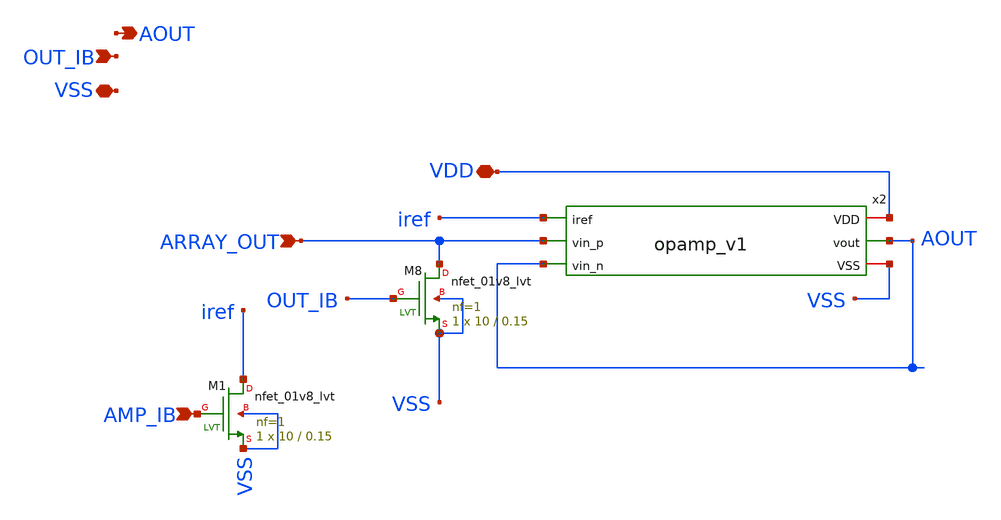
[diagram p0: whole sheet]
** sch_path: xschem/opamp_diego/opamp_wrapper.sch
**.subckt opamp_wrapper ARRAY_OUT AMP_IB VDD AOUT OUT_IB VSS
*.ipin ARRAY_OUT
*.ipin AMP_IB
*.iopin VDD
*.opin AOUT
*.ipin OUT_IB
*.iopin VSS
XM8 ARRAY_OUT OUT_IB VSS VSS sky130_fd_pr__nfet_01v8_lvt L=0.15 W=10 nf=1 ad='int((nf+1)/2) * W/nf * 0.29'
+ as='int((nf+2)/2) * W/nf * 0.29' pd='2*int((nf+1)/2) * (W/nf + 0.29)' ps='2*int((nf+2)/2) * (W/nf + 0.29)'
+ nrd='0.29 / W' nrs='0.29 / W' sa=0 sb=0 sd=0 mult=1 m=1
XM1 iref AMP_IB VSS VSS sky130_fd_pr__nfet_01v8_lvt L=0.15 W=10 nf=1 ad='int((nf+1)/2) * W/nf * 0.29'
+ as='int((nf+2)/2) * W/nf * 0.29' pd='2*int((nf+1)/2) * (W/nf + 0.29)' ps='2*int((nf+2)/2) * (W/nf + 0.29)'
+ nrd='0.29 / W' nrs='0.29 / W' sa=0 sb=0 sd=0 mult=1 m=1
x2 VDD iref ARRAY_OUT AOUT AOUT VSS opamp_v1
**.ends

* expanding   symbol:
*+  /home/hni/snrlab-ic-sky130-explorer-pixel-v0/Modules/uw_pixel/Schematic/opamp_diego/opamp_v1.sym # of pins=6
** sym_path: xschem/opamp_diego/opamp_v1.sym
** sch_path: xschem/opamp_diego/opamp_v1.sch
.subckt opamp_v1 VDD iref vin_p vin_n vout VSS
*.iopin VDD
*.iopin VSS
*.ipin iref
*.opin vout
*.ipin vin_n
*.ipin vin_p
XM1 net1 vin_n net3 net3 sky130_fd_pr__pfet_01v8 L=0.3 W=3 nf=1 ad='W * 0.29' as='W * 0.29' pd='2 * (W + 0.29)'
+ ps='2 * (W + 0.29)' nrd='0.29 / W' nrs='0.29 / W' sa=0 sb=0 sd=0 mult=200 m=200
XM2 net2 vin_p net3 net3 sky130_fd_pr__pfet_01v8 L=0.3 W=3 nf=1 ad='W * 0.29' as='W * 0.29' pd='2 * (W + 0.29)'
+ ps='2 * (W + 0.29)' nrd='0.29 / W' nrs='0.29 / W' sa=0 sb=0 sd=0 mult=200 m=200
XM3 net1 net1 VSS VSS sky130_fd_pr__nfet_01v8 L=0.3 W=3 nf=1 ad='W * 0.29' as='W * 0.29' pd='2 * (W + 0.29)'
+ ps='2 * (W + 0.29)' nrd='0.29 / W' nrs='0.29 / W' sa=0 sb=0 sd=0 mult=30 m=30
XM4 net2 net1 VSS VSS sky130_fd_pr__nfet_01v8 L=0.3 W=3 nf=1 ad='W * 0.29' as='W * 0.29' pd='2 * (W + 0.29)'
+ ps='2 * (W + 0.29)' nrd='0.29 / W' nrs='0.29 / W' sa=0 sb=0 sd=0 mult=30 m=30
XM5 net3 iref VDD VDD sky130_fd_pr__pfet_01v8 L=0.3 W=3 nf=1 ad='W * 0.29' as='W * 0.29' pd='2 * (W + 0.29)'
+ ps='2 * (W + 0.29)' nrd='0.29 / W' nrs='0.29 / W' sa=0 sb=0 sd=0 mult=30 m=30
XM7 vout iref VDD VDD sky130_fd_pr__pfet_01v8 L=0.3 W=3 nf=1 ad='W * 0.29' as='W * 0.29' pd='2 * (W + 0.29)'
+ ps='2 * (W + 0.29)' nrd='0.29 / W' nrs='0.29 / W' sa=0 sb=0 sd=0 mult=150 m=150
XM8 iref iref VDD VDD sky130_fd_pr__pfet_01v8 L=0.3 W=3 nf=1 ad='W * 0.29' as='W * 0.29' pd='2 * (W + 0.29)'
+ ps='2 * (W + 0.29)' nrd='0.29 / W' nrs='0.29 / W' sa=0 sb=0 sd=0 mult=15 m=15
XM9 net4 VDD net2 VSS sky130_fd_pr__nfet_01v8 L=0.15 W=0.75 nf=1 ad='W * 0.29' as='W * 0.29' pd='2 * (W + 0.29)'
+ ps='2 * (W + 0.29)' nrd='0.29 / W' nrs='0.29 / W' sa=0 sb=0 sd=0 mult=6 m=6
XC1 vout net4 sky130_fd_pr__cap_mim_m3_1 W=17.55 L=15 MF=6 m=6
XM6 vout net2 VSS VSS sky130_fd_pr__nfet_01v8 L=0.45 W=4.5 nf=1 ad='W * 0.29' as='W * 0.29' pd='2 * (W + 0.29)'
+ ps='2 * (W + 0.29)' nrd='0.29 / W' nrs='0.29 / W' sa=0 sb=0 sd=0 mult=150 m=150
.ends

.end
